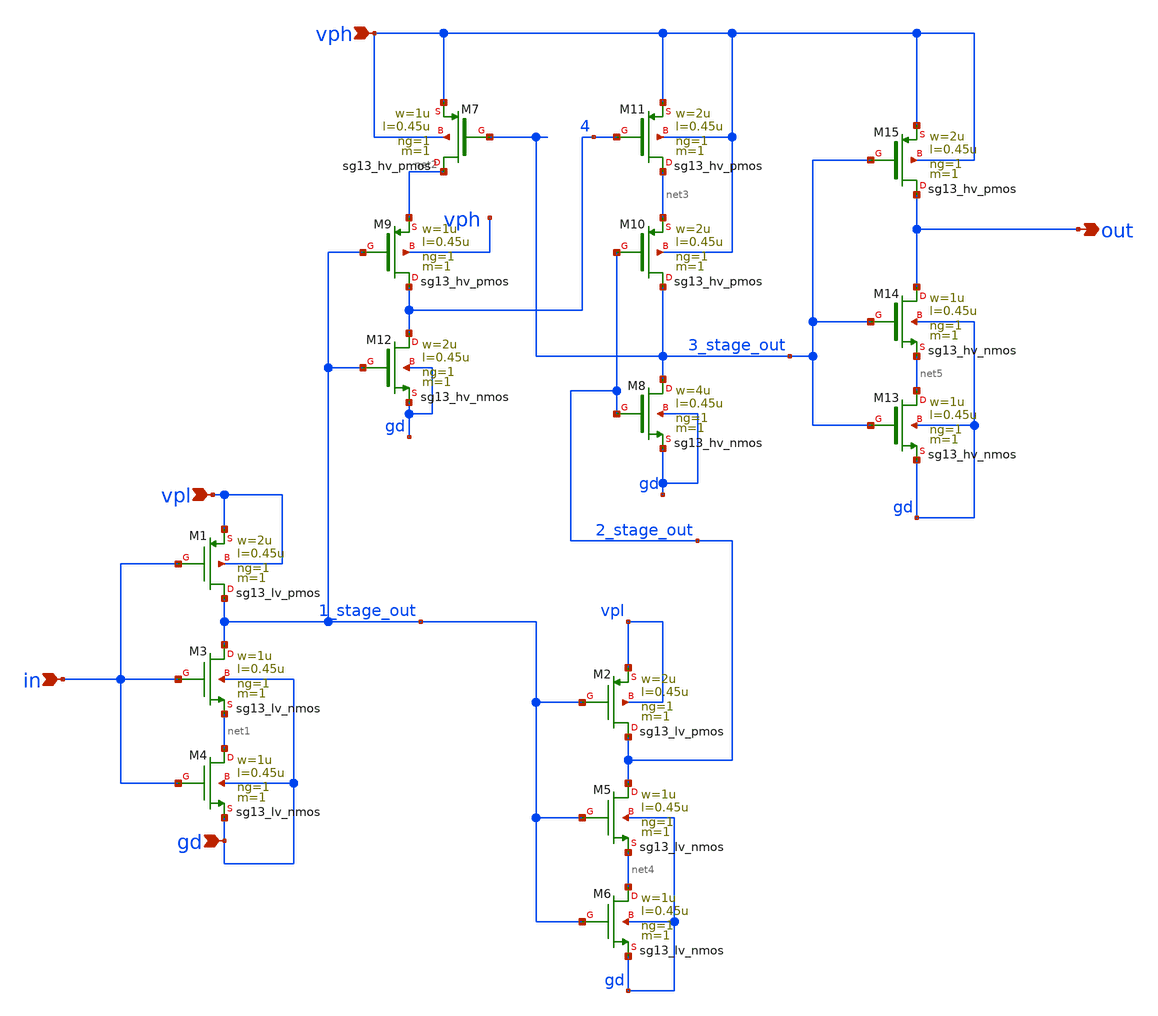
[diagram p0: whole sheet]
** sch_path: PLL0663-main/schematic/xschem/misc/debug_level_shifter.sch
**.subckt debug_level_shifter in out gd vph vpl
*.ipin in
*.opin out
*.ipin gd
*.ipin vph
*.ipin vpl
XM1 1_stage_out in vpl vpl sg13_lv_pmos w=2u l=0.45u ng=1 m=1 mm_ok=1
XM3 1_stage_out in net1 gd sg13_lv_nmos w=1u l=0.45u ng=1 m=1 mm_ok=1
XM4 net1 in gd gd sg13_lv_nmos w=1u l=0.45u ng=1 m=1 mm_ok=1
XM2 2_stage_out 1_stage_out vpl vpl sg13_lv_pmos w=2u l=0.45u ng=1 m=1 mm_ok=1
XM5 2_stage_out 1_stage_out net4 gd sg13_lv_nmos w=1u l=0.45u ng=1 m=1 mm_ok=1
XM6 net4 1_stage_out gd gd sg13_lv_nmos w=1u l=0.45u ng=1 m=1 mm_ok=1
XM7 net2 3_stage_out vph vph sg13_hv_pmos w=1u l=0.45u ng=1 m=1 mm_ok=1
XM8 3_stage_out 2_stage_out gd gd sg13_hv_nmos w=4u l=0.45u ng=1 m=1 mm_ok=1
XM9 4 1_stage_out net2 vph sg13_hv_pmos w=1u l=0.45u ng=1 m=1 mm_ok=1
XM10 3_stage_out 2_stage_out net3 vph sg13_hv_pmos w=2u l=0.45u ng=1 m=1 mm_ok=1
XM11 net3 4 vph vph sg13_hv_pmos w=2u l=0.45u ng=1 m=1 mm_ok=1
XM12 4 1_stage_out gd gd sg13_hv_nmos w=2u l=0.45u ng=1 m=1 mm_ok=1
XM15 out 3_stage_out vph vph sg13_hv_pmos w=2u l=0.45u ng=1 m=1 mm_ok=1
XM14 out 3_stage_out net5 gd sg13_hv_nmos w=1u l=0.45u ng=1 m=1 mm_ok=1
XM13 net5 3_stage_out gd gd sg13_hv_nmos w=1u l=0.45u ng=1 m=1 mm_ok=1
**.ends
.end
